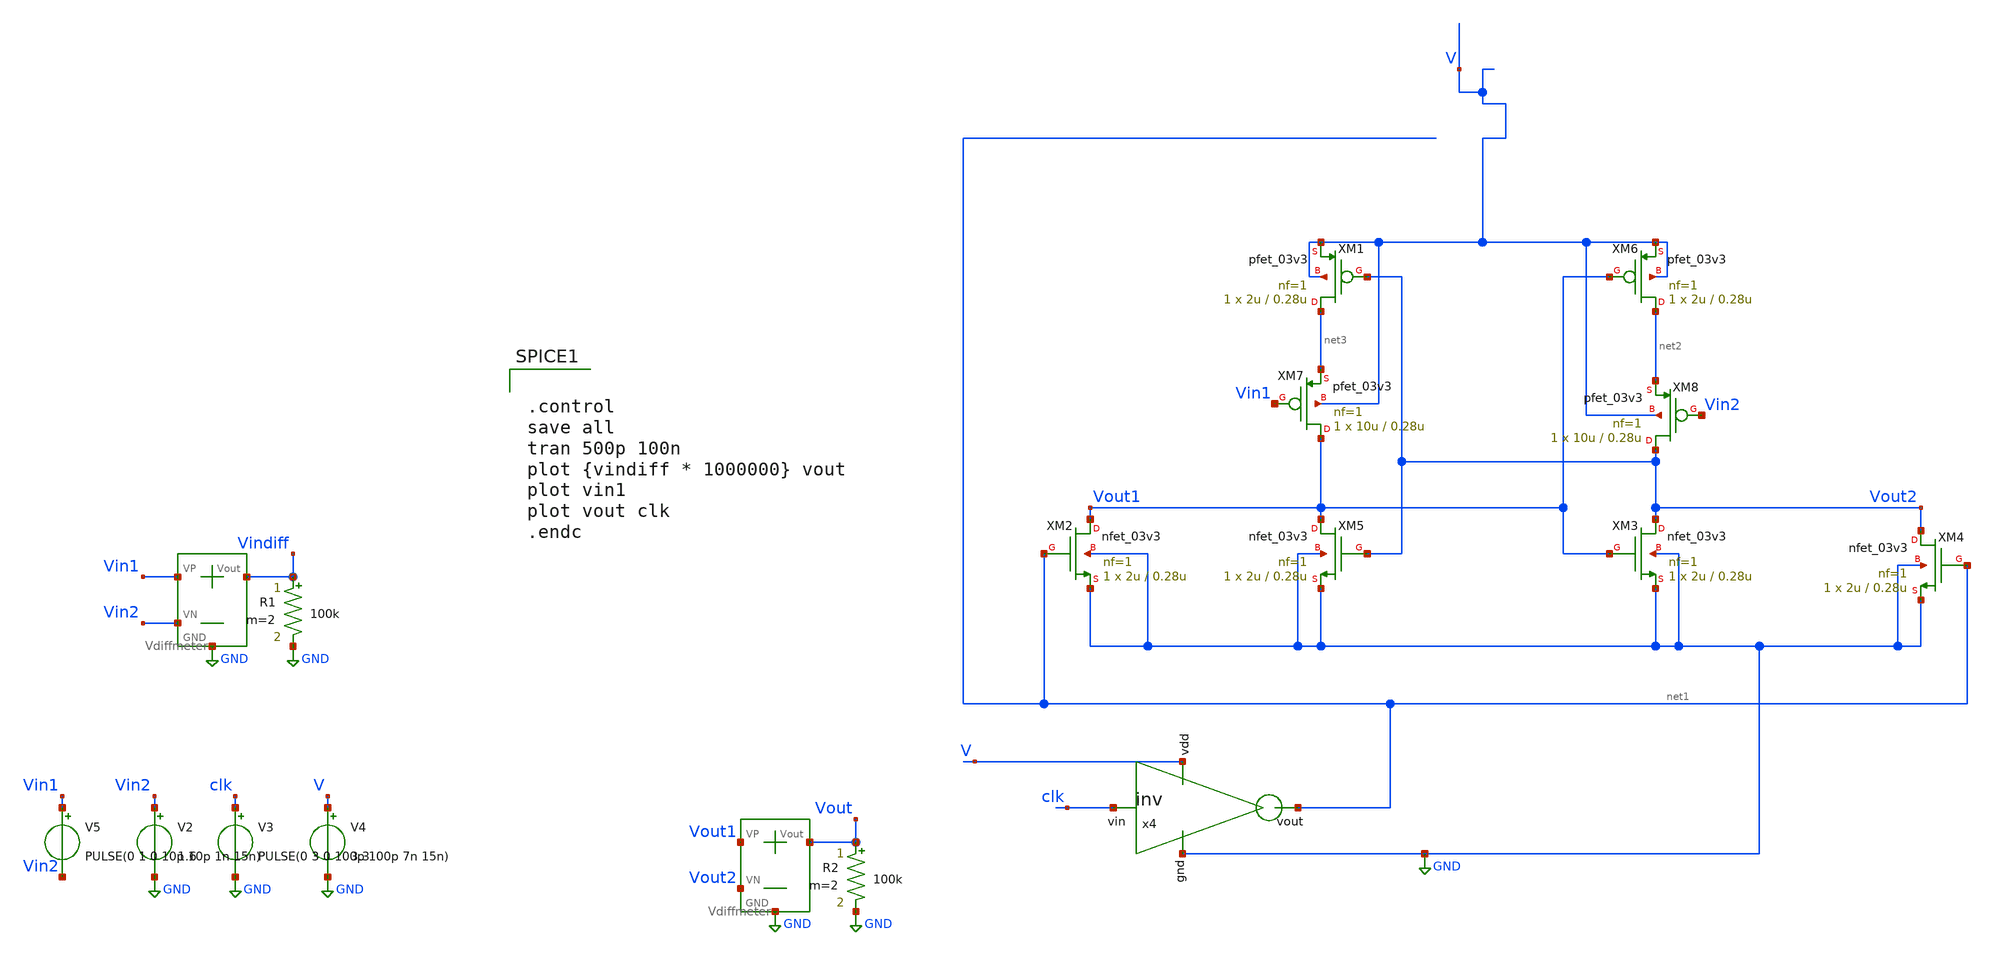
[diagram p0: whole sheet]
** sch_path: SAR_ADC/xschem/test/strongarm_tb/no symbol/peak__tb.sch
**.subckt peak__tb
V2 Vin2 GND 1.6
V3 clk GND PULSE(0 3 0 100p 100p 7n 15n)
V4 V GND 3.3
R1 Vindiff GND 100k m=2
R2 Vout GND 100k m=2
X3 Vout1 Vout2 Vout GND Vdiffmeter
X2 Vin1 Vin2 Vindiff GND Vdiffmeter
XM1 net3 Vout2 V V pfet_03v3 L=0.28u W=2u nf=1 ad='int((nf+1)/2) * W/nf * 0.18u' as='int((nf+2)/2) * W/nf * 0.18u'
+ pd='2*int((nf+1)/2) * (W/nf + 0.18u)' ps='2*int((nf+2)/2) * (W/nf + 0.18u)' nrd='0.18u / W' nrs='0.18u / W'
+ sa=0 sb=0 sd=0 m=1
XM2 Vout1 net1 GND GND nfet_03v3 L=0.28u W=2u nf=1 ad='int((nf+1)/2) * W/nf * 0.18u' as='int((nf+2)/2) * W/nf * 0.18u'
+ pd='2*int((nf+1)/2) * (W/nf + 0.18u)' ps='2*int((nf+2)/2) * (W/nf + 0.18u)' nrd='0.18u / W' nrs='0.18u / W'
+ sa=0 sb=0 sd=0 m=1
XM3 Vout2 Vout1 GND GND nfet_03v3 L=0.28u W=2u nf=1 ad='int((nf+1)/2) * W/nf * 0.18u' as='int((nf+2)/2) * W/nf * 0.18u'
+ pd='2*int((nf+1)/2) * (W/nf + 0.18u)' ps='2*int((nf+2)/2) * (W/nf + 0.18u)' nrd='0.18u / W' nrs='0.18u / W'
+ sa=0 sb=0 sd=0 m=1
XM4 Vout2 net1 GND GND nfet_03v3 L=0.28u W=2u nf=1 ad='int((nf+1)/2) * W/nf * 0.18u' as='int((nf+2)/2) * W/nf * 0.18u'
+ pd='2*int((nf+1)/2) * (W/nf + 0.18u)' ps='2*int((nf+2)/2) * (W/nf + 0.18u)' nrd='0.18u / W' nrs='0.18u / W'
+ sa=0 sb=0 sd=0 m=1
XM5 Vout1 Vout2 GND GND nfet_03v3 L=0.28u W=2u nf=1 ad='int((nf+1)/2) * W/nf * 0.18u' as='int((nf+2)/2) * W/nf * 0.18u'
+ pd='2*int((nf+1)/2) * (W/nf + 0.18u)' ps='2*int((nf+2)/2) * (W/nf + 0.18u)' nrd='0.18u / W' nrs='0.18u / W'
+ sa=0 sb=0 sd=0 m=1
XM6 net2 Vout1 V V pfet_03v3 L=0.28u W=2u nf=1 ad='int((nf+1)/2) * W/nf * 0.18u' as='int((nf+2)/2) * W/nf * 0.18u'
+ pd='2*int((nf+1)/2) * (W/nf + 0.18u)' ps='2*int((nf+2)/2) * (W/nf + 0.18u)' nrd='0.18u / W' nrs='0.18u / W'
+ sa=0 sb=0 sd=0 m=1
XM7 Vout1 Vin1 net3 V pfet_03v3 L=0.28u W=10u nf=1 ad='int((nf+1)/2) * W/nf * 0.18u' as='int((nf+2)/2) * W/nf * 0.18u'
+ pd='2*int((nf+1)/2) * (W/nf + 0.18u)' ps='2*int((nf+2)/2) * (W/nf + 0.18u)' nrd='0.18u / W' nrs='0.18u / W'
+ sa=0 sb=0 sd=0 m=1
XM8 Vout2 Vin2 net2 V pfet_03v3 L=0.28u W=10u nf=1 ad='int((nf+1)/2) * W/nf * 0.18u' as='int((nf+2)/2) * W/nf * 0.18u'
+ pd='2*int((nf+1)/2) * (W/nf + 0.18u)' ps='2*int((nf+2)/2) * (W/nf + 0.18u)' nrd='0.18u / W' nrs='0.18u / W'
+ sa=0 sb=0 sd=0 m=1
x4 V GND net1 clk inv cl=0.28u wp=0.44u wn=0.22u
V5 Vin1 Vin2 PULSE(0 1 0 10p 10p 1n 15n)
**** begin user architecture code


.control
save all
tran 500p 100n
plot {vindiff * 1000000} vout
plot vin1
plot vout clk
.endc


.include /foss/pdks/gf180mcuC/libs.tech/ngspice/design.ngspice
.lib /foss/pdks/gf180mcuC/libs.tech/ngspice/sm141064.ngspice typical

**** end user architecture code
**.ends

* expanding   symbol:  ../../../../symbols/Vdiffmeter.sym # of pins=4
** sym_path: SAR_ADC/xschem/spice/symbols/Vdiffmeter.sym
** sch_path: SAR_ADC/xschem/spice/symbols/Vdiffmeter.sch
.subckt Vdiffmeter VP VN Vout GND
*.iopin Vout
*.iopin GND
*.iopin VP
*.iopin VN
R4 Vout GND 1k m=1
E4 Vout GND VP VN 1
.ends


* expanding   symbol:  ../../../../symbols/inv.sym # of pins=4
** sym_path: SAR_ADC/xschem/spice/inv.sym
** sch_path: SAR_ADC/xschem/spice/inv.sch
.subckt inv vdd gnd vout vin  cl=0.28u wp=0.44u wn=0.22u
*.ipin gnd
*.ipin vdd
*.ipin vin
*.opin vout
XM1 gnd vin vout gnd nfet_03v3 L=0.28u W=4u nf=1 ad='int((nf+1)/2) * W/nf * 0.18u' as='int((nf+2)/2) * W/nf * 0.18u'
+ pd='2*int((nf+1)/2) * (W/nf + 0.18u)' ps='2*int((nf+2)/2) * (W/nf + 0.18u)' nrd='0.18u / W' nrs='0.18u / W'
+ sa=0 sb=0 sd=0 m=1
XM2 vdd vin vout vdd pfet_03v3 L=0.28u W=4u nf=1 ad='int((nf+1)/2) * W/nf * 0.18u' as='int((nf+2)/2) * W/nf * 0.18u'
+ pd='2*int((nf+1)/2) * (W/nf + 0.18u)' ps='2*int((nf+2)/2) * (W/nf + 0.18u)' nrd='0.18u / W' nrs='0.18u / W'
+ sa=0 sb=0 sd=0 m=1
.ends

.GLOBAL GND
.end
